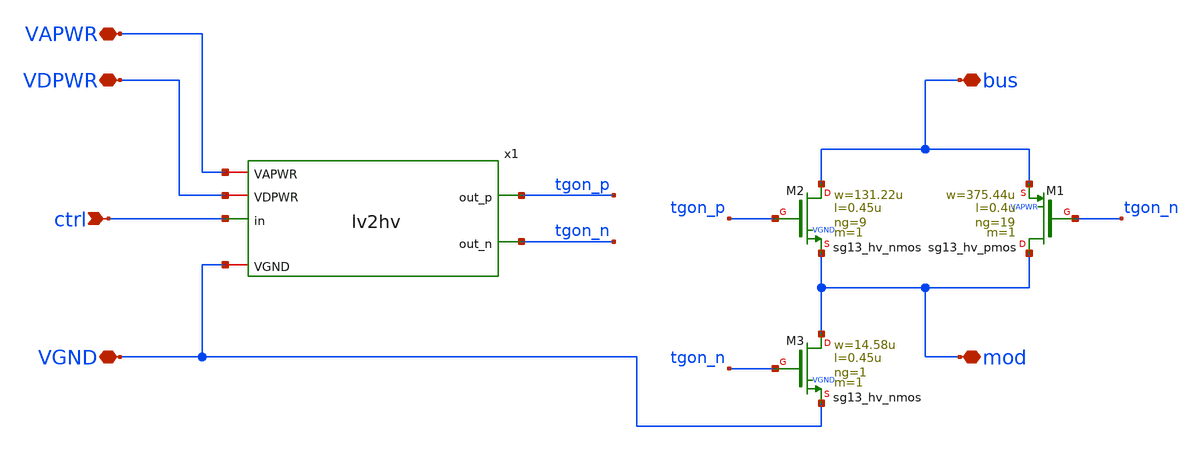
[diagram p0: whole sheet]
** sch_path: asw/ihp-sg13cmos5l/tt_asw_3v3/xschem/tt_asw_3v3.sch
**.subckt tt_asw_3v3 ctrl VDPWR VGND mod VAPWR bus
*.ipin ctrl
*.iopin VDPWR
*.iopin VGND
*.iopin mod
*.iopin VAPWR
*.iopin bus
x1 VGND VDPWR VAPWR ctrl tgon_p tgon_n lv2hv
XM1 mod tgon_n bus VAPWR sg13_hv_pmos w=375.44u l=0.4u ng=19 m=1
XM2 bus tgon_p mod VGND sg13_hv_nmos w=131.22u l=0.45u ng=9 m=1
XM3 mod tgon_n VGND VGND sg13_hv_nmos w=14.58u l=0.45u ng=1 m=1
**.ends
.end
